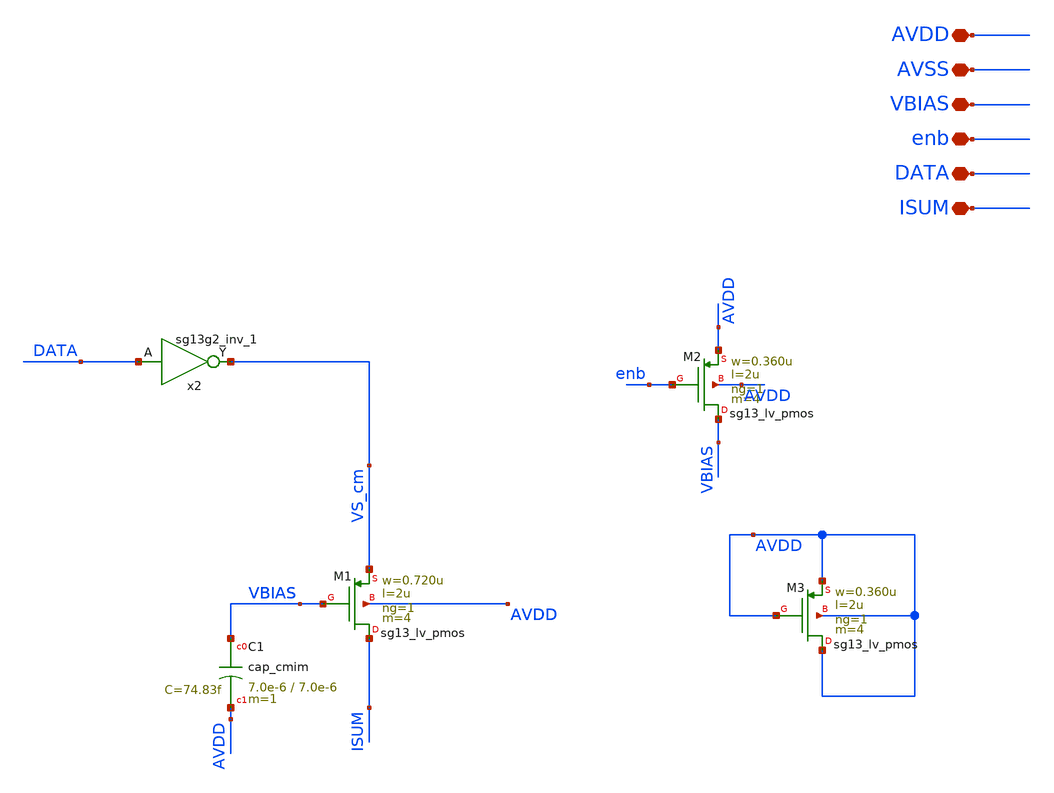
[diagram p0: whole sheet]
** sch_path: current_generator/analog/DAC/dac_bin_1.sch
**.subckt dac_bin_1 AVDD AVSS VBIAS enb DATA ISUM
*.iopin AVDD
*.iopin AVSS
*.iopin VBIAS
*.iopin enb
*.iopin DATA
*.iopin ISUM
XM1 ISUM VBIAS VS_cm AVDD sg13_lv_pmos w=0.720u l=2u ng=1 m=4 mm_ok=1
XC1 VBIAS AVDD cap_cmim w=7.0e-6 l=7.0e-6 m=1 mm_ok=1
XM2 VBIAS enb AVDD AVDD sg13_lv_pmos w=0.360u l=2u ng=1 m=4 mm_ok=1
XM3 AVDD AVDD AVDD AVDD sg13_lv_pmos w=0.360u l=2u ng=1 m=4 mm_ok=1
x2 VS_cm DATA AVDD AVSS sg13g2_inv_1
**.ends

* expanding   symbol:  sg13g2_stdcells/sg13g2_inv_1.sym # of pins=2
** sym_path: sg13g2_stdcells/sg13g2_inv_1.sym
** sch_path: sg13g2_stdcells/sg13g2_inv_1.sch
.subckt sg13g2_inv_1 Y A VDD VSS
*.opin Y
*.ipin A
*.iopin VDD
*.iopin VSS
XM1 Y A VSS VSS sg13_lv_nmos w=740.00n l=130.00n ng=1 m=1 mm_ok=1
XM2 Y A VDD VDD sg13_lv_pmos w=1.12u l=130.00n ng=1 m=1 mm_ok=1
.ends

.end
